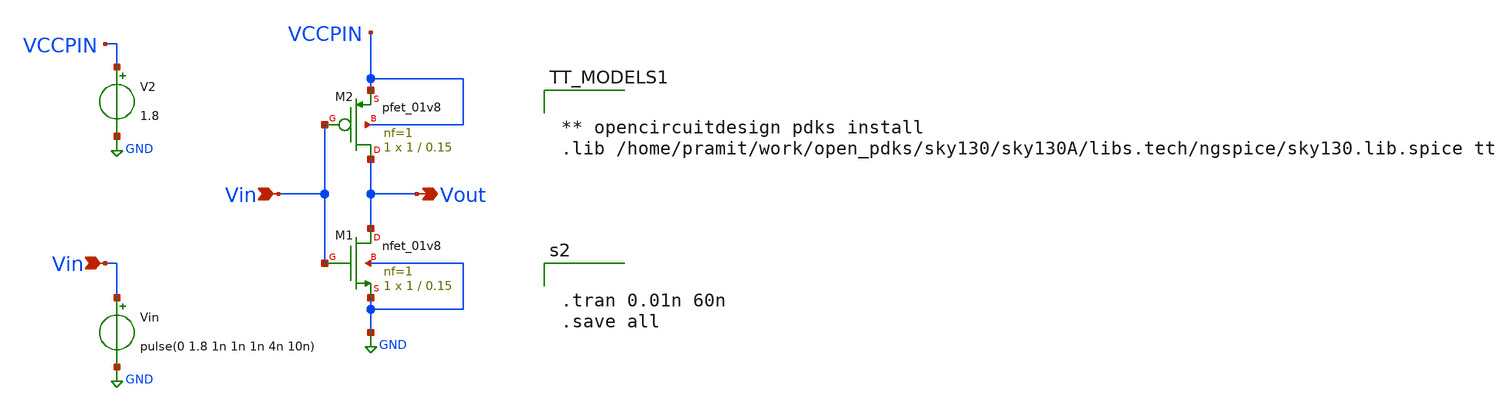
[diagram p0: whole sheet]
** sch_path: Week_1/inverter.sch
* Copyright 2021 Stefan Frederik Schippers
* Licensed under the Apache License, Version 2.0 (the "License");
* you may not use this file except in compliance with the License.
* You may obtain a copy of the License at
* https://www.apache.org/licenses/LICENSE-2.0
* Unless required by applicable law or agreed to in writing, software
* distributed under the License is distributed on an "AS IS" BASIS,
* WITHOUT WARRANTIES OR CONDITIONS OF ANY KIND, either express or implied.
* See the License for the specific language governing permissions and
* limitations under the License.
**.subckt inverter Vout Vin Vin
*.opin Vout
*.ipin Vin
*.ipin Vin
XM1 Vout Vin GND GND sky130_fd_pr__nfet_01v8 L=0.15 W=1 nf=1 ad='int((1 + 1)/2) * 1 / 1 * 0.29' as='int((1 + 2)/2) * 1 / 1 * 0.29'
+ pd='2*int((1 + 1)/2) * (1 / 1 + 0.29)' ps='2*int((1 + 2)/2) * (1 / 1 + 0.29)' nrd='0.29 / 1 ' nrs='0.29 / 1 '
+ sa=0 sb=0 sd=0 mult=1 m=1
XM2 Vout Vin VCCPIN VCCPIN sky130_fd_pr__pfet_01v8 L=0.15 W=1 nf=1 ad='int((nf+1)/2) * W/nf * 0.29' as='int((nf+2)/2) * W/nf * 0.29'
+ pd='2*int((nf+1)/2) * (W/nf + 0.29)' ps='2*int((nf+2)/2) * (W/nf + 0.29)' nrd='0.29 / W' nrs='0.29 / W'
+ sa=0 sb=0 sd=0 mult=1 m=1
Vin Vin GND pulse(0 1.8 1n 1n 1n 4n 10n)
V2 VCCPIN GND 1.8
**** begin user architecture code


.tran 0.01n 60n
.save all




** opencircuitdesign pdks install
.lib /home/pramit/work/open_pdks/sky130/sky130A/libs.tech/ngspice/sky130.lib.spice tt


**** end user architecture code
**.ends
.GLOBAL GND
.end
